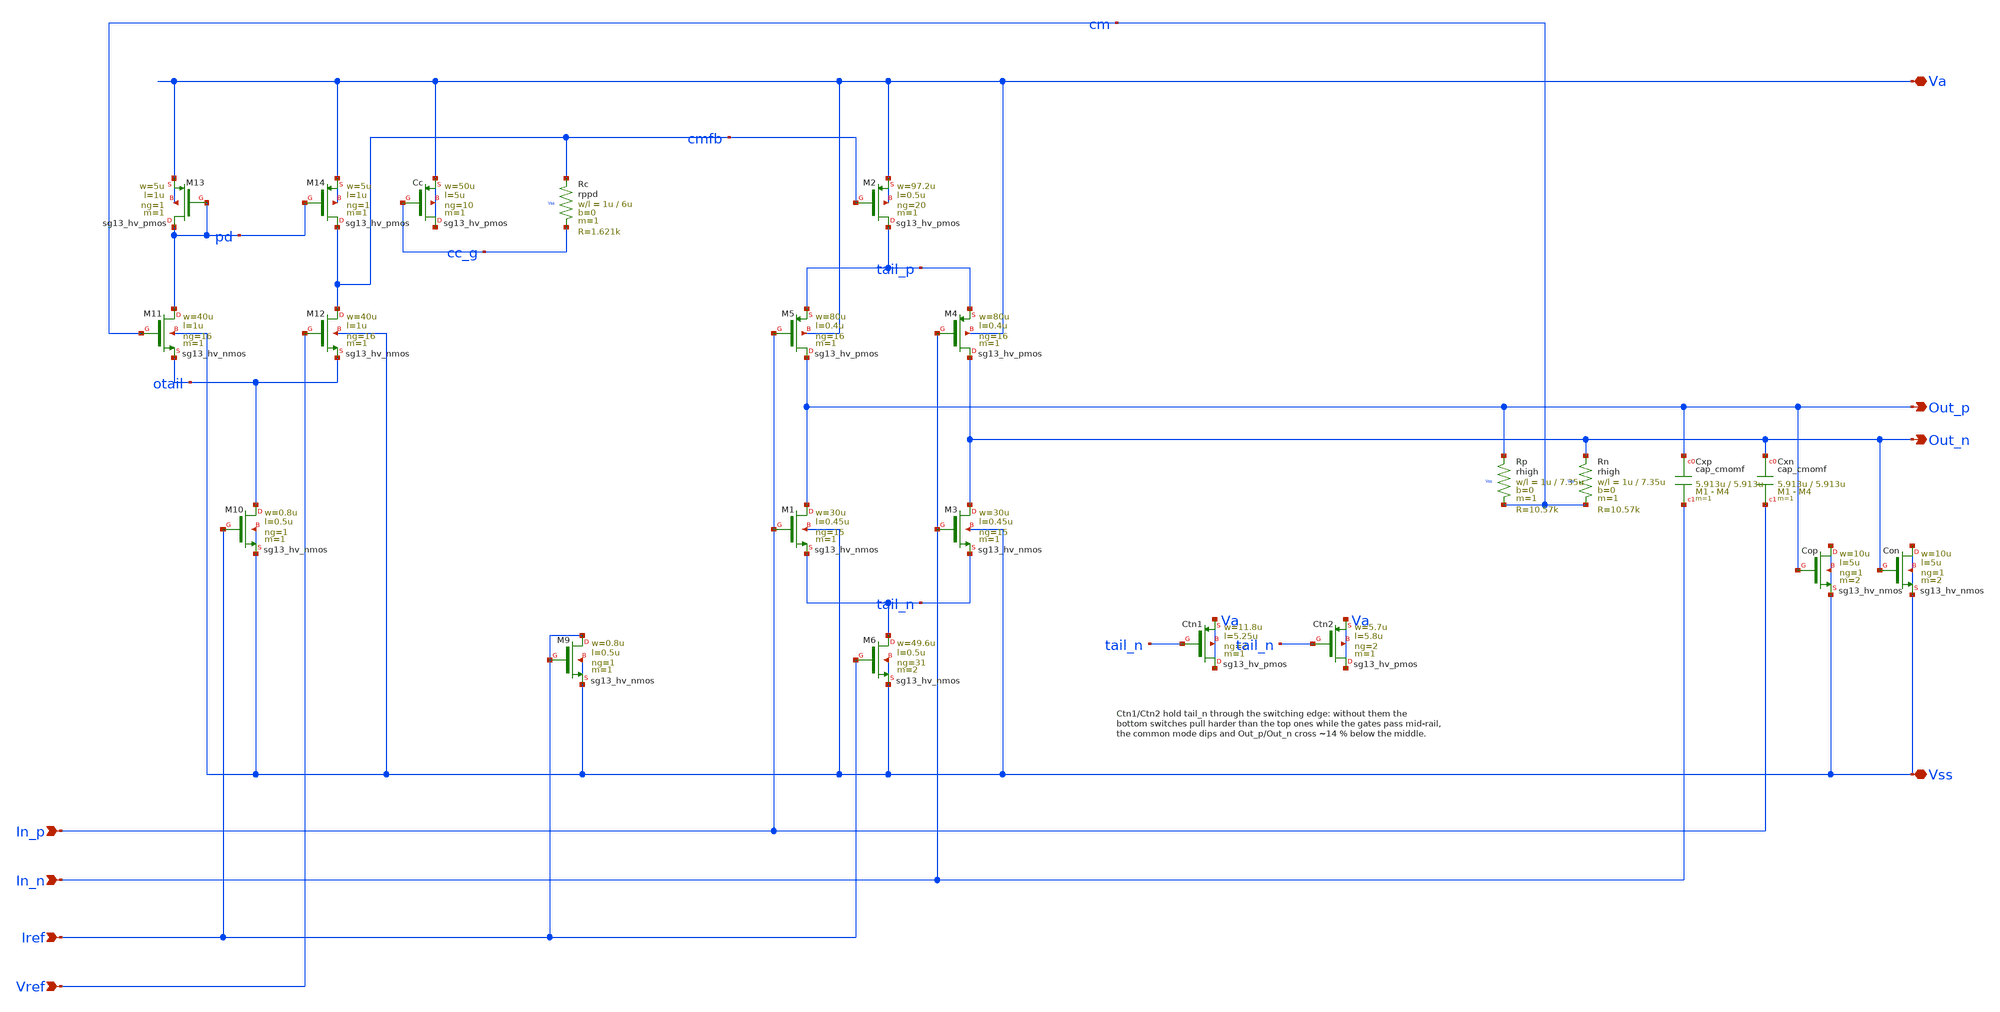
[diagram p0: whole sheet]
** sch_path: macros/lvds_tx/schematic/xschem/Driver.sch
**.subckt Driver Va Vss Out_p Out_n In_p In_n Iref Vref
*.iopin Va
*.iopin Vss
*.opin Out_p
*.opin Out_n
*.ipin In_p
*.ipin In_n
*.ipin Iref
*.ipin Vref
XCtn1 Va tail_n Va Va sg13_hv_pmos w=11.8u l=5.25u ng=2 m=1 mm_ok=1
XCtn2 Va tail_n Va Va sg13_hv_pmos w=5.7u l=5.8u ng=2 m=1 mm_ok=1
XM2 tail_p cmfb Va Va sg13_hv_pmos w=97.2u l=0.5u ng=20 m=1 mm_ok=1
XM5 Out_p In_p tail_p Va sg13_hv_pmos w=80u l=0.4u ng=16 m=1 mm_ok=1
XM4 Out_n In_n tail_p Va sg13_hv_pmos w=80u l=0.4u ng=16 m=1 mm_ok=1
XM1 Out_p In_p tail_n Vss sg13_hv_nmos w=30u l=0.45u ng=15 m=1 mm_ok=1
XM3 Out_n In_n tail_n Vss sg13_hv_nmos w=30u l=0.45u ng=15 m=1 mm_ok=1
XM6 tail_n Iref Vss Vss sg13_hv_nmos w=49.6u l=0.5u ng=31 m=2 mm_ok=1
XM9 Iref Iref Vss Vss sg13_hv_nmos w=0.8u l=0.5u ng=1 m=1 mm_ok=1
XM13 pd pd Va Va sg13_hv_pmos w=5u l=1u ng=1 m=1 mm_ok=1
XM14 cmfb pd Va Va sg13_hv_pmos w=5u l=1u ng=1 m=1 mm_ok=1
XM11 pd cm otail Vss sg13_hv_nmos w=40u l=1u ng=16 m=1 mm_ok=1
XM12 cmfb Vref otail Vss sg13_hv_nmos w=40u l=1u ng=16 m=1 mm_ok=1
XM10 otail Iref Vss Vss sg13_hv_nmos w=0.8u l=0.5u ng=1 m=1 mm_ok=1
XCc Va cc_g Va Va sg13_hv_pmos w=50u l=5u ng=10 m=1 mm_ok=1
XRc cmfb cc_g Vss rppd w=1u l=6u m=1 b=0 mm_ok=1
XRp Out_p cm Vss rhigh w=1u l=7.35u m=1 b=0 mm_ok=1
XRn Out_n cm Vss rhigh w=1u l=7.35u m=1 b=0 mm_ok=1
XCxp Out_p In_n cap_cmomf w=5.913u l=5.913u mmin=1 mmax=4 subblock=0 rfmodel=0 subscale=1 m=1
+ mm_ok=1
XCxn Out_n In_p cap_cmomf w=5.913u l=5.913u mmin=1 mmax=4 subblock=0 rfmodel=0 subscale=1 m=1
+ mm_ok=1
XCop Vss Out_p Vss Vss sg13_hv_nmos w=10u l=5u ng=1 m=2 mm_ok=1
XCon Vss Out_n Vss Vss sg13_hv_nmos w=10u l=5u ng=1 m=2 mm_ok=1
**.ends
.end
